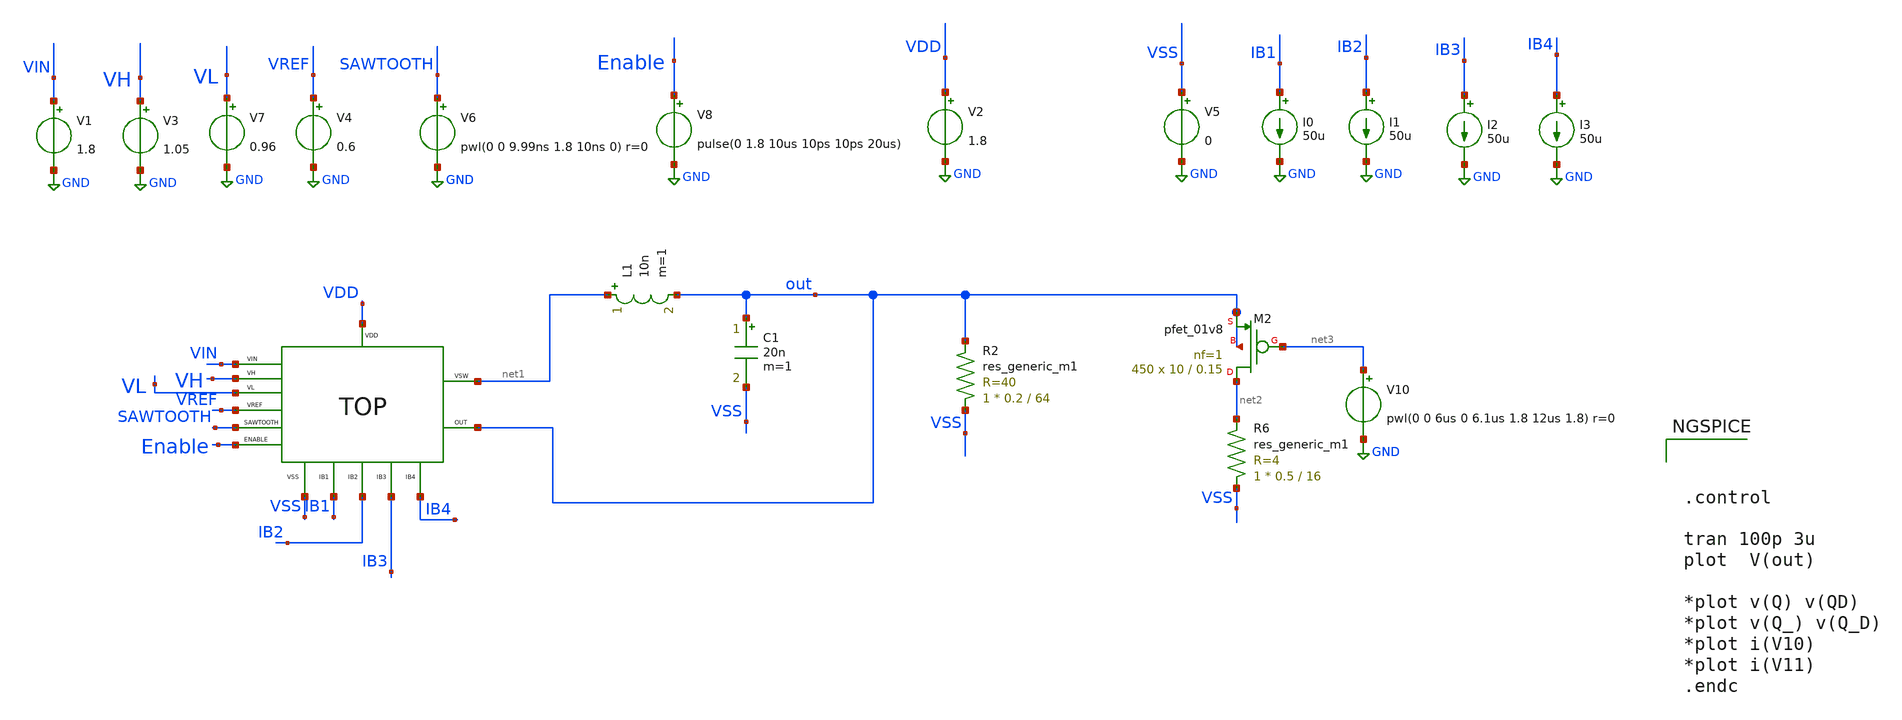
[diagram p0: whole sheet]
** sch_path: xschem/DC_DC_Converter_xschem/OTHERS/DC_DC_Converter_5/TOP_LEVEL/Top_TB.sch
**.subckt Top_TB
V1 VIN GND 1.8
I0 IB1 GND 50u
V2 VDD GND 1.8
V5 VSS GND 0
V4 VREF GND 0.6
I1 IB2 GND 50u
V6 SAWTOOTH GND pwl(0 0 9.99ns 1.8 10ns 0) r=0
V3 VH GND 1.05
V7 VL GND 0.96
I2 IB3 GND 50u
I3 IB4 GND 50u
V8 Enable GND pulse(0 1.8 10us 10ps 10ps 20us)
L1 net1 out 10n m=1
C1 out VSS 20n m=1
XM2 net2 net3 out out sky130_fd_pr__pfet_01v8 L=0.15 W=10 nf=1 ad='int((nf+1)/2) * W/nf * 0.29' as='int((nf+2)/2) * W/nf * 0.29'
+ pd='2*int((nf+1)/2) * (W/nf + 0.29)' ps='2*int((nf+2)/2) * (W/nf + 0.29)' nrd='0.29 / W' nrs='0.29 / W'
+ sa=0 sb=0 sd=0 mult=450 m=450
V10 net3 GND pwl(0 0 6us 0 6.1us 1.8 12us 1.8) r=0
R2 VSS out sky130_fd_pr__res_generic_m1 W=0.2 L=64 m=1
R6 VSS net2 sky130_fd_pr__res_generic_m1 W=0.5 L=16 m=1
x1 VDD net1 VIN VH out VREF VL SAWTOOTH Enable IB4 IB2 IB1 IB3 VSS Top
**** begin user architecture code

** opencircuitdesign pdks install
.lib $::SKYWATER_MODELS/sky130.lib.spice tt





.control

tran 100p 3u
plot  V(out)

*plot v(Q) v(QD)
*plot v(Q_) v(Q_D)
*plot i(V10)
*plot i(V11)
.endc


**** end user architecture code
**.ends
.GLOBAL GND
.end
